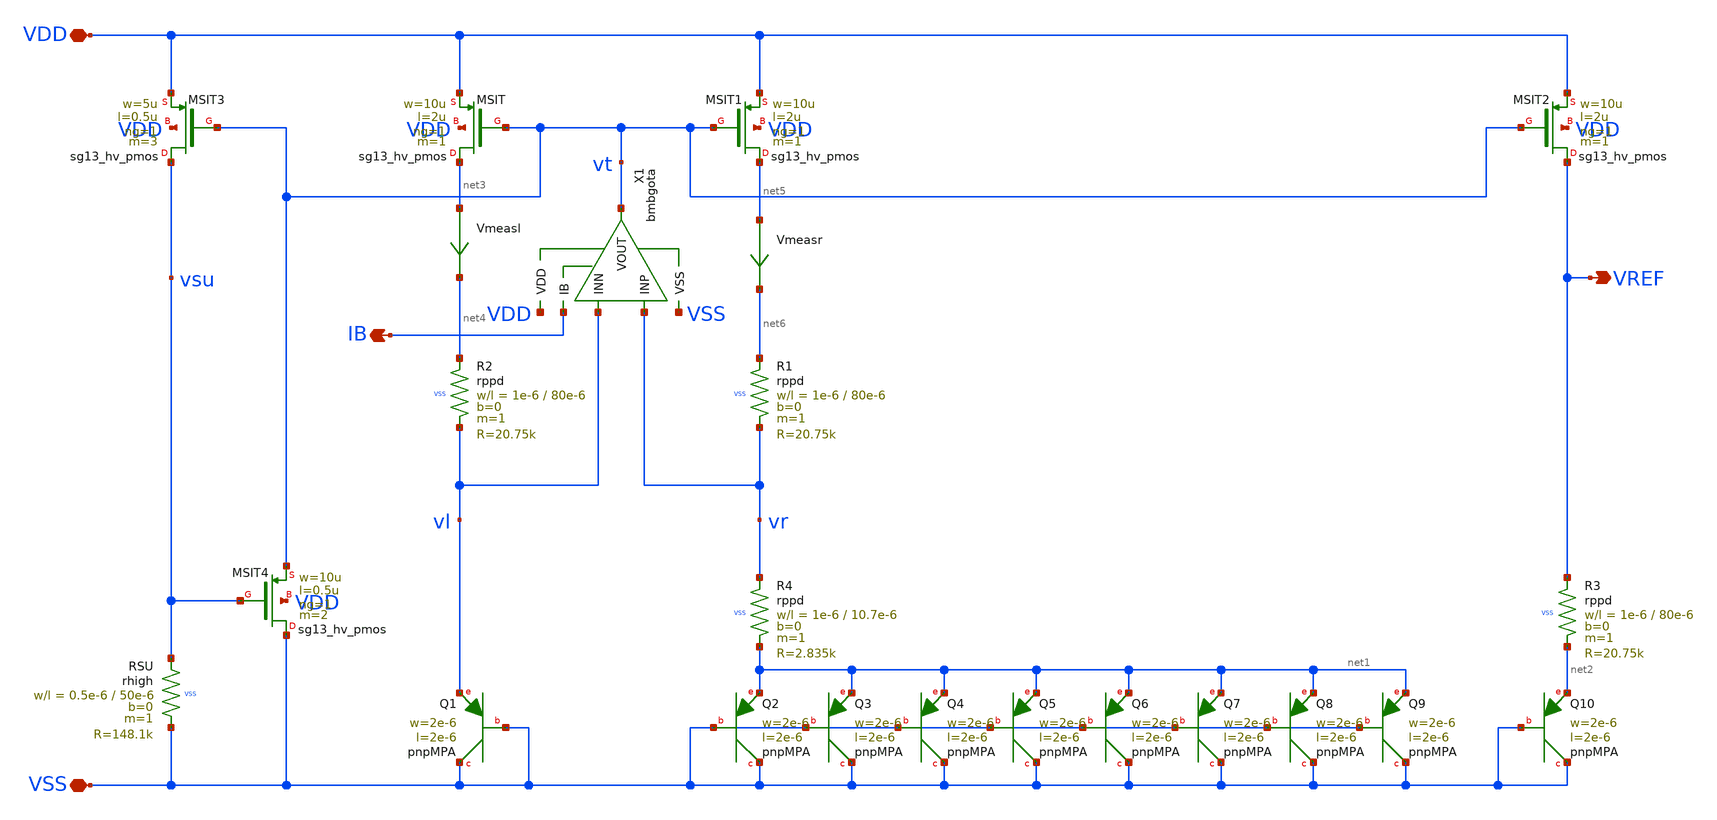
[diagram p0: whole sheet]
** sch_path: ip/bmbg/xschem/bmbg.sch
**.subckt bmbg VSS VDD VREF IB
*.iopin VSS
*.iopin VDD
*.opin VREF
*.opin IB
X1 VDD VSS vt IB vl vr bmbgota
XMSIT3 vsu vt VDD VDD sg13_hv_pmos w=5u l=0.5u ng=1 m=3 mm_ok=1
XMSIT4 VSS vsu vt VDD sg13_hv_pmos w=10u l=0.5u ng=1 m=2 mm_ok=1
XMSIT net3 vt VDD VDD sg13_hv_pmos w=10u l=2u ng=1 m=1 mm_ok=1
XMSIT1 net5 vt VDD VDD sg13_hv_pmos w=10u l=2u ng=1 m=1 mm_ok=1
XMSIT2 VREF vt VDD VDD sg13_hv_pmos w=10u l=2u ng=1 m=1 mm_ok=1
XQ1 VSS VSS vl pnpMPA a=4p p=8u m=1
XQ2 VSS VSS net1 pnpMPA a=4p p=8u m=1
XQ3 VSS VSS net1 pnpMPA a=4p p=8u m=1
XQ4 VSS VSS net1 pnpMPA a=4p p=8u m=1
XQ5 VSS VSS net1 pnpMPA a=4p p=8u m=1
XQ6 VSS VSS net1 pnpMPA a=4p p=8u m=1
XQ7 VSS VSS net1 pnpMPA a=4p p=8u m=1
XQ8 VSS VSS net1 pnpMPA a=4p p=8u m=1
XQ9 VSS VSS net1 pnpMPA a=4p p=8u m=1
XQ10 VSS VSS net2 pnpMPA a=4p p=8u m=1
Vmeasl net3 net4 0
.save i(vmeasl)
Vmeasr net5 net6 0
.save i(vmeasr)
XRSU vsu VSS VSS rhigh w=0.5e-6 l=50e-6 m=1 b=0 mm_ok=1
XR2 net4 vl VSS rppd w=1e-6 l=80e-6 m=1 b=0 mm_ok=1
XR1 net6 vr VSS rppd w=1e-6 l=80e-6 m=1 b=0 mm_ok=1
XR4 vr net1 VSS rppd w=1e-6 l=10.7e-6 m=1 b=0 mm_ok=1
XR3 VREF net2 VSS rppd w=1e-6 l=80e-6 m=1 b=0 mm_ok=1
**.ends

* expanding   symbol:  bmbgota.sym # of pins=6
** sym_path: ip/bmbg/xschem/bmbgota.sym
** sch_path: ip/bmbg/xschem/bmbgota.sch
.subckt bmbgota VDD VSS VOUT IB INN INP
*.iopin INP
*.iopin INN
*.iopin VOUT
*.opin IB
*.iopin VDD
*.iopin VSS
XMMIR1 IB IB VDD VDD sg13_hv_pmos w=5u l=2u ng=1 m=1 mm_ok=1
XMMIR2 net1 IB VDD VDD sg13_hv_pmos w=5u l=2u ng=1 m=2 mm_ok=1
XMMIR3 VOUT IB VDD VDD sg13_hv_pmos w=5u l=2u ng=1 m=3 mm_ok=1
XMDL net2 INN net1 VDD sg13_hv_pmos w=10u l=1u ng=1 m=16 mm_ok=1
XMDR net3 INP net1 VDD sg13_hv_pmos w=10u l=1u ng=1 m=16 mm_ok=1
XMMIRR net3 net2 VSS VSS sg13_hv_nmos w=5u l=2u ng=1 m=4 mm_ok=1
XMMIRL net2 net2 VSS VSS sg13_hv_nmos w=5u l=2u ng=1 m=4 mm_ok=1
XMO VOUT net3 VSS VSS sg13_hv_nmos w=5u l=2u ng=1 m=4 mm_ok=1
XC1 VOUT net4 cap_cmim w=30e-6 l=21e-6 m=1 mm_ok=1
XR1 net3 net4 VSS rhigh w=0.5e-6 l=3.5e-6 m=1 b=0 mm_ok=1
.ends

.end
